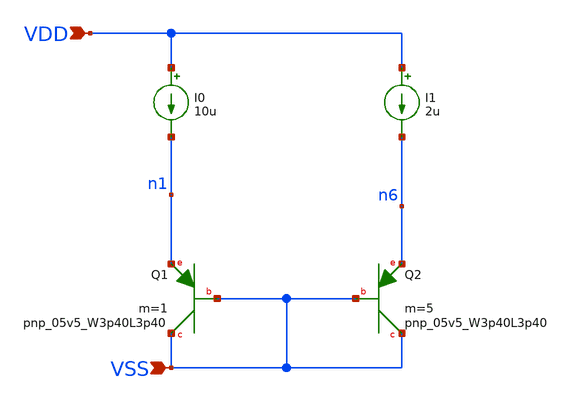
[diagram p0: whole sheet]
** sch_path: design/RPLY_EX0_SKY130NM/test1.sch
**.subckt test1 VDD VSS
*.ipin VDD
*.ipin VSS
I0 VDD n1 10u
I1 VDD n6 2u
XQ1 VSS VSS n1 sky130_fd_pr__pnp_05v5_W3p40L3p40 m=1
XQ2 VSS VSS n6 sky130_fd_pr__pnp_05v5_W3p40L3p40 m=5
**.ends
.end
